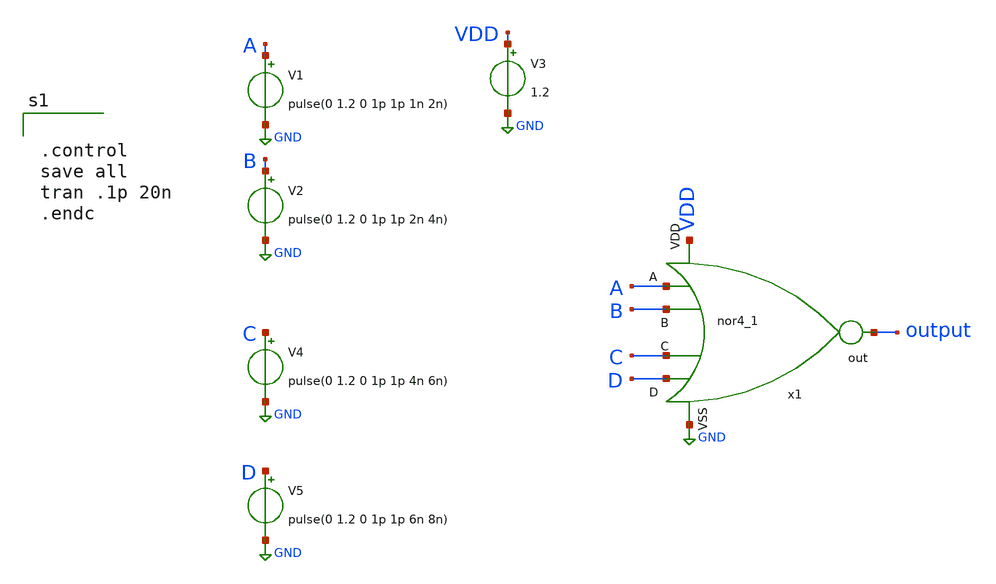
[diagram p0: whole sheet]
** sch_path: nor/nor4_tb.sch
**.subckt nor4_tb
x1 VDD A B C D output GND nor4
V1 A GND pulse(0 1.2 0 1p 1p 1n 2n)
V2 B GND pulse(0 1.2 0 1p 1p 2n 4n)
V3 VDD GND 1.2
V4 C GND pulse(0 1.2 0 1p 1p 4n 6n)
V5 D GND pulse(0 1.2 0 1p 1p 6n 8n)
**** begin user architecture code

** opencircuitdesign pdks install
.lib $::SKYWATER_MODELS/sky130.lib.spice tt




.control
save all
tran .1p 20n
.endc

**** end user architecture code
**.ends

* expanding   symbol:  nor4.sym # of pins=7
** sym_path: nor/nor4.sym
** sch_path: nor/nor4.sch
.subckt nor4 VDD A B C D out VSS
*.ipin A
*.ipin B
*.opin out
*.ipin VSS
*.ipin VDD
*.ipin C
*.ipin D
XM1 out B VSS VSS sky130_fd_pr__nfet_01v8 L=0.15 W=1 nf=1 ad='int((nf+1)/2) * W/nf * 0.29' as='int((nf+2)/2) * W/nf * 0.29'
+ pd='2*int((nf+1)/2) * (W/nf + 0.29)' ps='2*int((nf+2)/2) * (W/nf + 0.29)' nrd='0.29 / W' nrs='0.29 / W'
+ sa=0 sb=0 sd=0 mult=1 m=1
XM2 net2 B net1 net1 sky130_fd_pr__pfet_01v8 L=0.15 W=1 nf=1 ad='int((nf+1)/2) * W/nf * 0.29' as='int((nf+2)/2) * W/nf * 0.29'
+ pd='2*int((nf+1)/2) * (W/nf + 0.29)' ps='2*int((nf+2)/2) * (W/nf + 0.29)' nrd='0.29 / W' nrs='0.29 / W'
+ sa=0 sb=0 sd=0 mult=1 m=1
XM3 net1 A VDD VDD sky130_fd_pr__pfet_01v8 L=0.15 W=1 nf=1 ad='int((nf+1)/2) * W/nf * 0.29' as='int((nf+2)/2) * W/nf * 0.29'
+ pd='2*int((nf+1)/2) * (W/nf + 0.29)' ps='2*int((nf+2)/2) * (W/nf + 0.29)' nrd='0.29 / W' nrs='0.29 / W'
+ sa=0 sb=0 sd=0 mult=1 m=1
XM4 out A VSS VSS sky130_fd_pr__nfet_01v8 L=0.15 W=1 nf=1 ad='int((nf+1)/2) * W/nf * 0.29' as='int((nf+2)/2) * W/nf * 0.29'
+ pd='2*int((nf+1)/2) * (W/nf + 0.29)' ps='2*int((nf+2)/2) * (W/nf + 0.29)' nrd='0.29 / W' nrs='0.29 / W'
+ sa=0 sb=0 sd=0 mult=1 m=1
XM5 net3 C net2 net2 sky130_fd_pr__pfet_01v8 L=0.15 W=1 nf=1 ad='int((nf+1)/2) * W/nf * 0.29' as='int((nf+2)/2) * W/nf * 0.29'
+ pd='2*int((nf+1)/2) * (W/nf + 0.29)' ps='2*int((nf+2)/2) * (W/nf + 0.29)' nrd='0.29 / W' nrs='0.29 / W'
+ sa=0 sb=0 sd=0 mult=1 m=1
XM6 out C VSS VSS sky130_fd_pr__nfet_01v8 L=0.15 W=1 nf=1 ad='int((nf+1)/2) * W/nf * 0.29' as='int((nf+2)/2) * W/nf * 0.29'
+ pd='2*int((nf+1)/2) * (W/nf + 0.29)' ps='2*int((nf+2)/2) * (W/nf + 0.29)' nrd='0.29 / W' nrs='0.29 / W'
+ sa=0 sb=0 sd=0 mult=1 m=1
XM7 out D VSS VSS sky130_fd_pr__nfet_01v8 L=0.15 W=1 nf=1 ad='int((nf+1)/2) * W/nf * 0.29' as='int((nf+2)/2) * W/nf * 0.29'
+ pd='2*int((nf+1)/2) * (W/nf + 0.29)' ps='2*int((nf+2)/2) * (W/nf + 0.29)' nrd='0.29 / W' nrs='0.29 / W'
+ sa=0 sb=0 sd=0 mult=1 m=1
XM8 out D net3 net3 sky130_fd_pr__pfet_01v8 L=0.15 W=1 nf=1 ad='int((nf+1)/2) * W/nf * 0.29' as='int((nf+2)/2) * W/nf * 0.29'
+ pd='2*int((nf+1)/2) * (W/nf + 0.29)' ps='2*int((nf+2)/2) * (W/nf + 0.29)' nrd='0.29 / W' nrs='0.29 / W'
+ sa=0 sb=0 sd=0 mult=1 m=1
.ends

.GLOBAL GND
.end
